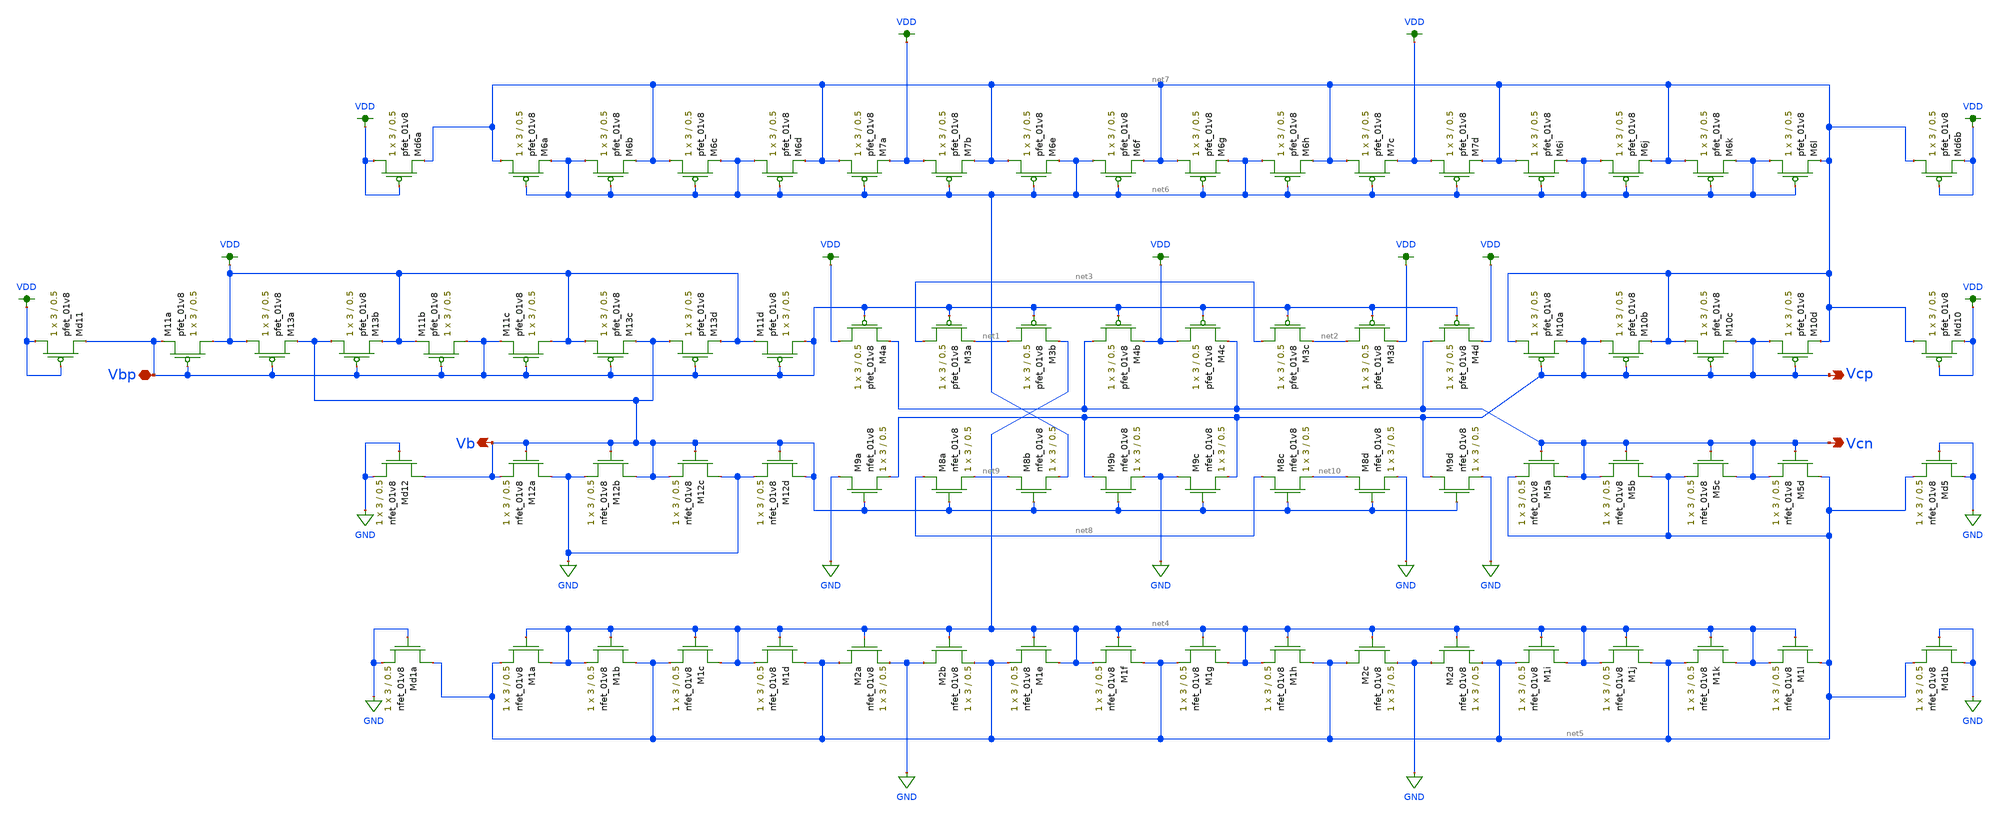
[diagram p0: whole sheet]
** sch_path: mp3/xschem/bias_layout.sch
**.subckt bias_layout Vcp Vbp Vcn Vb
*.opin Vcp
*.iopin Vbp
*.opin Vcn
*.opin Vb
XM1a net4 net4 net5 GND sky130_fd_pr__nfet_01v8 L=0.5 W=3 nf=1 ad='int((nf+1)/2) * W/nf * 0.29' as='int((nf+2)/2) * W/nf * 0.29'
+ pd='2*int((nf+1)/2) * (W/nf + 0.29)' ps='2*int((nf+2)/2) * (W/nf + 0.29)' nrd='0.29 / W' nrs='0.29 / W'
+ sa=0 sb=0 sd=0 mult=1 m=1
XM1b net5 net4 net4 GND sky130_fd_pr__nfet_01v8 L=0.5 W=3 nf=1 ad='int((nf+1)/2) * W/nf * 0.29' as='int((nf+2)/2) * W/nf * 0.29'
+ pd='2*int((nf+1)/2) * (W/nf + 0.29)' ps='2*int((nf+2)/2) * (W/nf + 0.29)' nrd='0.29 / W' nrs='0.29 / W'
+ sa=0 sb=0 sd=0 mult=1 m=1
XM1c net4 net4 net5 GND sky130_fd_pr__nfet_01v8 L=0.5 W=3 nf=1 ad='int((nf+1)/2) * W/nf * 0.29' as='int((nf+2)/2) * W/nf * 0.29'
+ pd='2*int((nf+1)/2) * (W/nf + 0.29)' ps='2*int((nf+2)/2) * (W/nf + 0.29)' nrd='0.29 / W' nrs='0.29 / W'
+ sa=0 sb=0 sd=0 mult=1 m=1
XM1d net5 net4 net4 GND sky130_fd_pr__nfet_01v8 L=0.5 W=3 nf=1 ad='int((nf+1)/2) * W/nf * 0.29' as='int((nf+2)/2) * W/nf * 0.29'
+ pd='2*int((nf+1)/2) * (W/nf + 0.29)' ps='2*int((nf+2)/2) * (W/nf + 0.29)' nrd='0.29 / W' nrs='0.29 / W'
+ sa=0 sb=0 sd=0 mult=1 m=1
XM2a net5 net4 GND GND sky130_fd_pr__nfet_01v8 L=0.5 W=3 nf=1 ad='int((nf+1)/2) * W/nf * 0.29' as='int((nf+2)/2) * W/nf * 0.29'
+ pd='2*int((nf+1)/2) * (W/nf + 0.29)' ps='2*int((nf+2)/2) * (W/nf + 0.29)' nrd='0.29 / W' nrs='0.29 / W'
+ sa=0 sb=0 sd=0 mult=1 m=1
XM2b GND net4 net5 GND sky130_fd_pr__nfet_01v8 L=0.5 W=3 nf=1 ad='int((nf+1)/2) * W/nf * 0.29' as='int((nf+2)/2) * W/nf * 0.29'
+ pd='2*int((nf+1)/2) * (W/nf + 0.29)' ps='2*int((nf+2)/2) * (W/nf + 0.29)' nrd='0.29 / W' nrs='0.29 / W'
+ sa=0 sb=0 sd=0 mult=1 m=1
XM2c net5 net4 GND GND sky130_fd_pr__nfet_01v8 L=0.5 W=3 nf=1 ad='int((nf+1)/2) * W/nf * 0.29' as='int((nf+2)/2) * W/nf * 0.29'
+ pd='2*int((nf+1)/2) * (W/nf + 0.29)' ps='2*int((nf+2)/2) * (W/nf + 0.29)' nrd='0.29 / W' nrs='0.29 / W'
+ sa=0 sb=0 sd=0 mult=1 m=1
XM2d GND net4 net5 GND sky130_fd_pr__nfet_01v8 L=0.5 W=3 nf=1 ad='int((nf+1)/2) * W/nf * 0.29' as='int((nf+2)/2) * W/nf * 0.29'
+ pd='2*int((nf+1)/2) * (W/nf + 0.29)' ps='2*int((nf+2)/2) * (W/nf + 0.29)' nrd='0.29 / W' nrs='0.29 / W'
+ sa=0 sb=0 sd=0 mult=1 m=1
XM3a net3 Vbp net1 VDD sky130_fd_pr__pfet_01v8 L=0.5 W=3 nf=1 ad='int((nf+1)/2) * W/nf * 0.29' as='int((nf+2)/2) * W/nf * 0.29'
+ pd='2*int((nf+1)/2) * (W/nf + 0.29)' ps='2*int((nf+2)/2) * (W/nf + 0.29)' nrd='0.29 / W' nrs='0.29 / W'
+ sa=0 sb=0 sd=0 mult=1 m=1
XM3b net1 Vbp net4 VDD sky130_fd_pr__pfet_01v8 L=0.5 W=3 nf=1 ad='int((nf+1)/2) * W/nf * 0.29' as='int((nf+2)/2) * W/nf * 0.29'
+ pd='2*int((nf+1)/2) * (W/nf + 0.29)' ps='2*int((nf+2)/2) * (W/nf + 0.29)' nrd='0.29 / W' nrs='0.29 / W'
+ sa=0 sb=0 sd=0 mult=1 m=1
XM3c net3 Vbp net2 VDD sky130_fd_pr__pfet_01v8 L=0.5 W=3 nf=1 ad='int((nf+1)/2) * W/nf * 0.29' as='int((nf+2)/2) * W/nf * 0.29'
+ pd='2*int((nf+1)/2) * (W/nf + 0.29)' ps='2*int((nf+2)/2) * (W/nf + 0.29)' nrd='0.29 / W' nrs='0.29 / W'
+ sa=0 sb=0 sd=0 mult=1 m=1
XM3d net2 Vbp VDD VDD sky130_fd_pr__pfet_01v8 L=0.5 W=3 nf=1 ad='int((nf+1)/2) * W/nf * 0.29' as='int((nf+2)/2) * W/nf * 0.29'
+ pd='2*int((nf+1)/2) * (W/nf + 0.29)' ps='2*int((nf+2)/2) * (W/nf + 0.29)' nrd='0.29 / W' nrs='0.29 / W'
+ sa=0 sb=0 sd=0 mult=1 m=1
XM4a VDD Vbp Vcn VDD sky130_fd_pr__pfet_01v8 L=0.5 W=3 nf=1 ad='int((nf+1)/2) * W/nf * 0.29' as='int((nf+2)/2) * W/nf * 0.29'
+ pd='2*int((nf+1)/2) * (W/nf + 0.29)' ps='2*int((nf+2)/2) * (W/nf + 0.29)' nrd='0.29 / W' nrs='0.29 / W'
+ sa=0 sb=0 sd=0 mult=1 m=1
XM4b Vcn Vbp VDD VDD sky130_fd_pr__pfet_01v8 L=0.5 W=3 nf=1 ad='int((nf+1)/2) * W/nf * 0.29' as='int((nf+2)/2) * W/nf * 0.29'
+ pd='2*int((nf+1)/2) * (W/nf + 0.29)' ps='2*int((nf+2)/2) * (W/nf + 0.29)' nrd='0.29 / W' nrs='0.29 / W'
+ sa=0 sb=0 sd=0 mult=1 m=1
XM4c VDD Vbp Vcn VDD sky130_fd_pr__pfet_01v8 L=0.5 W=3 nf=1 ad='int((nf+1)/2) * W/nf * 0.29' as='int((nf+2)/2) * W/nf * 0.29'
+ pd='2*int((nf+1)/2) * (W/nf + 0.29)' ps='2*int((nf+2)/2) * (W/nf + 0.29)' nrd='0.29 / W' nrs='0.29 / W'
+ sa=0 sb=0 sd=0 mult=1 m=1
XM4d Vcn Vbp VDD VDD sky130_fd_pr__pfet_01v8 L=0.5 W=3 nf=1 ad='int((nf+1)/2) * W/nf * 0.29' as='int((nf+2)/2) * W/nf * 0.29'
+ pd='2*int((nf+1)/2) * (W/nf + 0.29)' ps='2*int((nf+2)/2) * (W/nf + 0.29)' nrd='0.29 / W' nrs='0.29 / W'
+ sa=0 sb=0 sd=0 mult=1 m=1
XM11a VDD Vbp Vbp VDD sky130_fd_pr__pfet_01v8 L=0.5 W=3 nf=1 ad='int((nf+1)/2) * W/nf * 0.29' as='int((nf+2)/2) * W/nf * 0.29'
+ pd='2*int((nf+1)/2) * (W/nf + 0.29)' ps='2*int((nf+2)/2) * (W/nf + 0.29)' nrd='0.29 / W' nrs='0.29 / W'
+ sa=0 sb=0 sd=0 mult=1 m=1
XM11b Vbp Vbp VDD VDD sky130_fd_pr__pfet_01v8 L=0.5 W=3 nf=1 ad='int((nf+1)/2) * W/nf * 0.29' as='int((nf+2)/2) * W/nf * 0.29'
+ pd='2*int((nf+1)/2) * (W/nf + 0.29)' ps='2*int((nf+2)/2) * (W/nf + 0.29)' nrd='0.29 / W' nrs='0.29 / W'
+ sa=0 sb=0 sd=0 mult=1 m=1
XM11c VDD Vbp Vbp VDD sky130_fd_pr__pfet_01v8 L=0.5 W=3 nf=1 ad='int((nf+1)/2) * W/nf * 0.29' as='int((nf+2)/2) * W/nf * 0.29'
+ pd='2*int((nf+1)/2) * (W/nf + 0.29)' ps='2*int((nf+2)/2) * (W/nf + 0.29)' nrd='0.29 / W' nrs='0.29 / W'
+ sa=0 sb=0 sd=0 mult=1 m=1
XM11d Vbp Vbp VDD VDD sky130_fd_pr__pfet_01v8 L=0.5 W=3 nf=1 ad='int((nf+1)/2) * W/nf * 0.29' as='int((nf+2)/2) * W/nf * 0.29'
+ pd='2*int((nf+1)/2) * (W/nf + 0.29)' ps='2*int((nf+2)/2) * (W/nf + 0.29)' nrd='0.29 / W' nrs='0.29 / W'
+ sa=0 sb=0 sd=0 mult=1 m=1
XM5a Vcn Vcn net5 GND sky130_fd_pr__nfet_01v8 L=0.5 W=3 nf=1 ad='int((nf+1)/2) * W/nf * 0.29' as='int((nf+2)/2) * W/nf * 0.29'
+ pd='2*int((nf+1)/2) * (W/nf + 0.29)' ps='2*int((nf+2)/2) * (W/nf + 0.29)' nrd='0.29 / W' nrs='0.29 / W'
+ sa=0 sb=0 sd=0 mult=1 m=1
XM5b net5 Vcn Vcn GND sky130_fd_pr__nfet_01v8 L=0.5 W=3 nf=1 ad='int((nf+1)/2) * W/nf * 0.29' as='int((nf+2)/2) * W/nf * 0.29'
+ pd='2*int((nf+1)/2) * (W/nf + 0.29)' ps='2*int((nf+2)/2) * (W/nf + 0.29)' nrd='0.29 / W' nrs='0.29 / W'
+ sa=0 sb=0 sd=0 mult=1 m=1
XM5c Vcn Vcn net5 GND sky130_fd_pr__nfet_01v8 L=0.5 W=3 nf=1 ad='int((nf+1)/2) * W/nf * 0.29' as='int((nf+2)/2) * W/nf * 0.29'
+ pd='2*int((nf+1)/2) * (W/nf + 0.29)' ps='2*int((nf+2)/2) * (W/nf + 0.29)' nrd='0.29 / W' nrs='0.29 / W'
+ sa=0 sb=0 sd=0 mult=1 m=1
XM5d net5 Vcn Vcn GND sky130_fd_pr__nfet_01v8 L=0.5 W=3 nf=1 ad='int((nf+1)/2) * W/nf * 0.29' as='int((nf+2)/2) * W/nf * 0.29'
+ pd='2*int((nf+1)/2) * (W/nf + 0.29)' ps='2*int((nf+2)/2) * (W/nf + 0.29)' nrd='0.29 / W' nrs='0.29 / W'
+ sa=0 sb=0 sd=0 mult=1 m=1
XM8a net8 Vb net9 GND sky130_fd_pr__nfet_01v8 L=0.5 W=3 nf=1 ad='int((nf+1)/2) * W/nf * 0.29' as='int((nf+2)/2) * W/nf * 0.29'
+ pd='2*int((nf+1)/2) * (W/nf + 0.29)' ps='2*int((nf+2)/2) * (W/nf + 0.29)' nrd='0.29 / W' nrs='0.29 / W'
+ sa=0 sb=0 sd=0 mult=1 m=1
XM8b net9 Vb net6 GND sky130_fd_pr__nfet_01v8 L=0.5 W=3 nf=1 ad='int((nf+1)/2) * W/nf * 0.29' as='int((nf+2)/2) * W/nf * 0.29'
+ pd='2*int((nf+1)/2) * (W/nf + 0.29)' ps='2*int((nf+2)/2) * (W/nf + 0.29)' nrd='0.29 / W' nrs='0.29 / W'
+ sa=0 sb=0 sd=0 mult=1 m=1
XM8c net8 Vb net10 GND sky130_fd_pr__nfet_01v8 L=0.5 W=3 nf=1 ad='int((nf+1)/2) * W/nf * 0.29' as='int((nf+2)/2) * W/nf * 0.29'
+ pd='2*int((nf+1)/2) * (W/nf + 0.29)' ps='2*int((nf+2)/2) * (W/nf + 0.29)' nrd='0.29 / W' nrs='0.29 / W'
+ sa=0 sb=0 sd=0 mult=1 m=1
XM8d net10 Vb GND GND sky130_fd_pr__nfet_01v8 L=0.5 W=3 nf=1 ad='int((nf+1)/2) * W/nf * 0.29' as='int((nf+2)/2) * W/nf * 0.29'
+ pd='2*int((nf+1)/2) * (W/nf + 0.29)' ps='2*int((nf+2)/2) * (W/nf + 0.29)' nrd='0.29 / W' nrs='0.29 / W'
+ sa=0 sb=0 sd=0 mult=1 m=1
XM6a net7 net6 net6 VDD sky130_fd_pr__pfet_01v8 L=0.5 W=3 nf=1 ad='int((nf+1)/2) * W/nf * 0.29' as='int((nf+2)/2) * W/nf * 0.29'
+ pd='2*int((nf+1)/2) * (W/nf + 0.29)' ps='2*int((nf+2)/2) * (W/nf + 0.29)' nrd='0.29 / W' nrs='0.29 / W'
+ sa=0 sb=0 sd=0 mult=1 m=1
XM6b net6 net6 net7 VDD sky130_fd_pr__pfet_01v8 L=0.5 W=3 nf=1 ad='int((nf+1)/2) * W/nf * 0.29' as='int((nf+2)/2) * W/nf * 0.29'
+ pd='2*int((nf+1)/2) * (W/nf + 0.29)' ps='2*int((nf+2)/2) * (W/nf + 0.29)' nrd='0.29 / W' nrs='0.29 / W'
+ sa=0 sb=0 sd=0 mult=1 m=1
XM6c net7 net6 net6 VDD sky130_fd_pr__pfet_01v8 L=0.5 W=3 nf=1 ad='int((nf+1)/2) * W/nf * 0.29' as='int((nf+2)/2) * W/nf * 0.29'
+ pd='2*int((nf+1)/2) * (W/nf + 0.29)' ps='2*int((nf+2)/2) * (W/nf + 0.29)' nrd='0.29 / W' nrs='0.29 / W'
+ sa=0 sb=0 sd=0 mult=1 m=1
XM6d net6 net6 net7 VDD sky130_fd_pr__pfet_01v8 L=0.5 W=3 nf=1 ad='int((nf+1)/2) * W/nf * 0.29' as='int((nf+2)/2) * W/nf * 0.29'
+ pd='2*int((nf+1)/2) * (W/nf + 0.29)' ps='2*int((nf+2)/2) * (W/nf + 0.29)' nrd='0.29 / W' nrs='0.29 / W'
+ sa=0 sb=0 sd=0 mult=1 m=1
XM7a net7 net6 VDD VDD sky130_fd_pr__pfet_01v8 L=0.5 W=3 nf=1 ad='int((nf+1)/2) * W/nf * 0.29' as='int((nf+2)/2) * W/nf * 0.29'
+ pd='2*int((nf+1)/2) * (W/nf + 0.29)' ps='2*int((nf+2)/2) * (W/nf + 0.29)' nrd='0.29 / W' nrs='0.29 / W'
+ sa=0 sb=0 sd=0 mult=1 m=1
XM7b VDD net6 net7 VDD sky130_fd_pr__pfet_01v8 L=0.5 W=3 nf=1 ad='int((nf+1)/2) * W/nf * 0.29' as='int((nf+2)/2) * W/nf * 0.29'
+ pd='2*int((nf+1)/2) * (W/nf + 0.29)' ps='2*int((nf+2)/2) * (W/nf + 0.29)' nrd='0.29 / W' nrs='0.29 / W'
+ sa=0 sb=0 sd=0 mult=1 m=1
XM7c net7 net6 VDD VDD sky130_fd_pr__pfet_01v8 L=0.5 W=3 nf=1 ad='int((nf+1)/2) * W/nf * 0.29' as='int((nf+2)/2) * W/nf * 0.29'
+ pd='2*int((nf+1)/2) * (W/nf + 0.29)' ps='2*int((nf+2)/2) * (W/nf + 0.29)' nrd='0.29 / W' nrs='0.29 / W'
+ sa=0 sb=0 sd=0 mult=1 m=1
XM7d VDD net6 net7 VDD sky130_fd_pr__pfet_01v8 L=0.5 W=3 nf=1 ad='int((nf+1)/2) * W/nf * 0.29' as='int((nf+2)/2) * W/nf * 0.29'
+ pd='2*int((nf+1)/2) * (W/nf + 0.29)' ps='2*int((nf+2)/2) * (W/nf + 0.29)' nrd='0.29 / W' nrs='0.29 / W'
+ sa=0 sb=0 sd=0 mult=1 m=1
XM10d Vcp Vcp net7 VDD sky130_fd_pr__pfet_01v8 L=0.5 W=3 nf=1 ad='int((nf+1)/2) * W/nf * 0.29' as='int((nf+2)/2) * W/nf * 0.29'
+ pd='2*int((nf+1)/2) * (W/nf + 0.29)' ps='2*int((nf+2)/2) * (W/nf + 0.29)' nrd='0.29 / W' nrs='0.29 / W'
+ sa=0 sb=0 sd=0 mult=1 m=1
XM10c net7 Vcp Vcp VDD sky130_fd_pr__pfet_01v8 L=0.5 W=3 nf=1 ad='int((nf+1)/2) * W/nf * 0.29' as='int((nf+2)/2) * W/nf * 0.29'
+ pd='2*int((nf+1)/2) * (W/nf + 0.29)' ps='2*int((nf+2)/2) * (W/nf + 0.29)' nrd='0.29 / W' nrs='0.29 / W'
+ sa=0 sb=0 sd=0 mult=1 m=1
XM10b Vcp Vcp net7 VDD sky130_fd_pr__pfet_01v8 L=0.5 W=3 nf=1 ad='int((nf+1)/2) * W/nf * 0.29' as='int((nf+2)/2) * W/nf * 0.29'
+ pd='2*int((nf+1)/2) * (W/nf + 0.29)' ps='2*int((nf+2)/2) * (W/nf + 0.29)' nrd='0.29 / W' nrs='0.29 / W'
+ sa=0 sb=0 sd=0 mult=1 m=1
XM10a net7 Vcp Vcp VDD sky130_fd_pr__pfet_01v8 L=0.5 W=3 nf=1 ad='int((nf+1)/2) * W/nf * 0.29' as='int((nf+2)/2) * W/nf * 0.29'
+ pd='2*int((nf+1)/2) * (W/nf + 0.29)' ps='2*int((nf+2)/2) * (W/nf + 0.29)' nrd='0.29 / W' nrs='0.29 / W'
+ sa=0 sb=0 sd=0 mult=1 m=1
XM9a GND Vb Vcp GND sky130_fd_pr__nfet_01v8 L=0.5 W=3 nf=1 ad='int((nf+1)/2) * W/nf * 0.29' as='int((nf+2)/2) * W/nf * 0.29'
+ pd='2*int((nf+1)/2) * (W/nf + 0.29)' ps='2*int((nf+2)/2) * (W/nf + 0.29)' nrd='0.29 / W' nrs='0.29 / W'
+ sa=0 sb=0 sd=0 mult=1 m=1
XM9b Vcp Vb GND GND sky130_fd_pr__nfet_01v8 L=0.5 W=3 nf=1 ad='int((nf+1)/2) * W/nf * 0.29' as='int((nf+2)/2) * W/nf * 0.29'
+ pd='2*int((nf+1)/2) * (W/nf + 0.29)' ps='2*int((nf+2)/2) * (W/nf + 0.29)' nrd='0.29 / W' nrs='0.29 / W'
+ sa=0 sb=0 sd=0 mult=1 m=1
XM9c GND Vb Vcp GND sky130_fd_pr__nfet_01v8 L=0.5 W=3 nf=1 ad='int((nf+1)/2) * W/nf * 0.29' as='int((nf+2)/2) * W/nf * 0.29'
+ pd='2*int((nf+1)/2) * (W/nf + 0.29)' ps='2*int((nf+2)/2) * (W/nf + 0.29)' nrd='0.29 / W' nrs='0.29 / W'
+ sa=0 sb=0 sd=0 mult=1 m=1
XM9d Vcp Vb GND GND sky130_fd_pr__nfet_01v8 L=0.5 W=3 nf=1 ad='int((nf+1)/2) * W/nf * 0.29' as='int((nf+2)/2) * W/nf * 0.29'
+ pd='2*int((nf+1)/2) * (W/nf + 0.29)' ps='2*int((nf+2)/2) * (W/nf + 0.29)' nrd='0.29 / W' nrs='0.29 / W'
+ sa=0 sb=0 sd=0 mult=1 m=1
XM12a GND Vb Vb GND sky130_fd_pr__nfet_01v8 L=0.5 W=3 nf=1 ad='int((nf+1)/2) * W/nf * 0.29' as='int((nf+2)/2) * W/nf * 0.29'
+ pd='2*int((nf+1)/2) * (W/nf + 0.29)' ps='2*int((nf+2)/2) * (W/nf + 0.29)' nrd='0.29 / W' nrs='0.29 / W'
+ sa=0 sb=0 sd=0 mult=1 m=1
XM12b Vb Vb GND GND sky130_fd_pr__nfet_01v8 L=0.5 W=3 nf=1 ad='int((nf+1)/2) * W/nf * 0.29' as='int((nf+2)/2) * W/nf * 0.29'
+ pd='2*int((nf+1)/2) * (W/nf + 0.29)' ps='2*int((nf+2)/2) * (W/nf + 0.29)' nrd='0.29 / W' nrs='0.29 / W'
+ sa=0 sb=0 sd=0 mult=1 m=1
XM12c GND Vb Vb GND sky130_fd_pr__nfet_01v8 L=0.5 W=3 nf=1 ad='int((nf+1)/2) * W/nf * 0.29' as='int((nf+2)/2) * W/nf * 0.29'
+ pd='2*int((nf+1)/2) * (W/nf + 0.29)' ps='2*int((nf+2)/2) * (W/nf + 0.29)' nrd='0.29 / W' nrs='0.29 / W'
+ sa=0 sb=0 sd=0 mult=1 m=1
XM12d Vb Vb GND GND sky130_fd_pr__nfet_01v8 L=0.5 W=3 nf=1 ad='int((nf+1)/2) * W/nf * 0.29' as='int((nf+2)/2) * W/nf * 0.29'
+ pd='2*int((nf+1)/2) * (W/nf + 0.29)' ps='2*int((nf+2)/2) * (W/nf + 0.29)' nrd='0.29 / W' nrs='0.29 / W'
+ sa=0 sb=0 sd=0 mult=1 m=1
XM13d Vb Vbp VDD VDD sky130_fd_pr__pfet_01v8 L=0.5 W=3 nf=1 ad='int((nf+1)/2) * W/nf * 0.29' as='int((nf+2)/2) * W/nf * 0.29'
+ pd='2*int((nf+1)/2) * (W/nf + 0.29)' ps='2*int((nf+2)/2) * (W/nf + 0.29)' nrd='0.29 / W' nrs='0.29 / W'
+ sa=0 sb=0 sd=0 mult=1 m=1
XM13c VDD Vbp Vb VDD sky130_fd_pr__pfet_01v8 L=0.5 W=3 nf=1 ad='int((nf+1)/2) * W/nf * 0.29' as='int((nf+2)/2) * W/nf * 0.29'
+ pd='2*int((nf+1)/2) * (W/nf + 0.29)' ps='2*int((nf+2)/2) * (W/nf + 0.29)' nrd='0.29 / W' nrs='0.29 / W'
+ sa=0 sb=0 sd=0 mult=1 m=1
XM13b Vb Vbp VDD VDD sky130_fd_pr__pfet_01v8 L=0.5 W=3 nf=1 ad='int((nf+1)/2) * W/nf * 0.29' as='int((nf+2)/2) * W/nf * 0.29'
+ pd='2*int((nf+1)/2) * (W/nf + 0.29)' ps='2*int((nf+2)/2) * (W/nf + 0.29)' nrd='0.29 / W' nrs='0.29 / W'
+ sa=0 sb=0 sd=0 mult=1 m=1
XM13a VDD Vbp Vb VDD sky130_fd_pr__pfet_01v8 L=0.5 W=3 nf=1 ad='int((nf+1)/2) * W/nf * 0.29' as='int((nf+2)/2) * W/nf * 0.29'
+ pd='2*int((nf+1)/2) * (W/nf + 0.29)' ps='2*int((nf+2)/2) * (W/nf + 0.29)' nrd='0.29 / W' nrs='0.29 / W'
+ sa=0 sb=0 sd=0 mult=1 m=1
XM1e net4 net4 net5 GND sky130_fd_pr__nfet_01v8 L=0.5 W=3 nf=1 ad='int((nf+1)/2) * W/nf * 0.29' as='int((nf+2)/2) * W/nf * 0.29'
+ pd='2*int((nf+1)/2) * (W/nf + 0.29)' ps='2*int((nf+2)/2) * (W/nf + 0.29)' nrd='0.29 / W' nrs='0.29 / W'
+ sa=0 sb=0 sd=0 mult=1 m=1
XM1f net5 net4 net4 GND sky130_fd_pr__nfet_01v8 L=0.5 W=3 nf=1 ad='int((nf+1)/2) * W/nf * 0.29' as='int((nf+2)/2) * W/nf * 0.29'
+ pd='2*int((nf+1)/2) * (W/nf + 0.29)' ps='2*int((nf+2)/2) * (W/nf + 0.29)' nrd='0.29 / W' nrs='0.29 / W'
+ sa=0 sb=0 sd=0 mult=1 m=1
XM1g net4 net4 net5 GND sky130_fd_pr__nfet_01v8 L=0.5 W=3 nf=1 ad='int((nf+1)/2) * W/nf * 0.29' as='int((nf+2)/2) * W/nf * 0.29'
+ pd='2*int((nf+1)/2) * (W/nf + 0.29)' ps='2*int((nf+2)/2) * (W/nf + 0.29)' nrd='0.29 / W' nrs='0.29 / W'
+ sa=0 sb=0 sd=0 mult=1 m=1
XM1h net5 net4 net4 GND sky130_fd_pr__nfet_01v8 L=0.5 W=3 nf=1 ad='int((nf+1)/2) * W/nf * 0.29' as='int((nf+2)/2) * W/nf * 0.29'
+ pd='2*int((nf+1)/2) * (W/nf + 0.29)' ps='2*int((nf+2)/2) * (W/nf + 0.29)' nrd='0.29 / W' nrs='0.29 / W'
+ sa=0 sb=0 sd=0 mult=1 m=1
XM6e net7 net6 net6 VDD sky130_fd_pr__pfet_01v8 L=0.5 W=3 nf=1 ad='int((nf+1)/2) * W/nf * 0.29' as='int((nf+2)/2) * W/nf * 0.29'
+ pd='2*int((nf+1)/2) * (W/nf + 0.29)' ps='2*int((nf+2)/2) * (W/nf + 0.29)' nrd='0.29 / W' nrs='0.29 / W'
+ sa=0 sb=0 sd=0 mult=1 m=1
XM6f net6 net6 net7 VDD sky130_fd_pr__pfet_01v8 L=0.5 W=3 nf=1 ad='int((nf+1)/2) * W/nf * 0.29' as='int((nf+2)/2) * W/nf * 0.29'
+ pd='2*int((nf+1)/2) * (W/nf + 0.29)' ps='2*int((nf+2)/2) * (W/nf + 0.29)' nrd='0.29 / W' nrs='0.29 / W'
+ sa=0 sb=0 sd=0 mult=1 m=1
XM6g net7 net6 net6 VDD sky130_fd_pr__pfet_01v8 L=0.5 W=3 nf=1 ad='int((nf+1)/2) * W/nf * 0.29' as='int((nf+2)/2) * W/nf * 0.29'
+ pd='2*int((nf+1)/2) * (W/nf + 0.29)' ps='2*int((nf+2)/2) * (W/nf + 0.29)' nrd='0.29 / W' nrs='0.29 / W'
+ sa=0 sb=0 sd=0 mult=1 m=1
XM6h net6 net6 net7 VDD sky130_fd_pr__pfet_01v8 L=0.5 W=3 nf=1 ad='int((nf+1)/2) * W/nf * 0.29' as='int((nf+2)/2) * W/nf * 0.29'
+ pd='2*int((nf+1)/2) * (W/nf + 0.29)' ps='2*int((nf+2)/2) * (W/nf + 0.29)' nrd='0.29 / W' nrs='0.29 / W'
+ sa=0 sb=0 sd=0 mult=1 m=1
XM1i net4 net4 net5 GND sky130_fd_pr__nfet_01v8 L=0.5 W=3 nf=1 ad='int((nf+1)/2) * W/nf * 0.29' as='int((nf+2)/2) * W/nf * 0.29'
+ pd='2*int((nf+1)/2) * (W/nf + 0.29)' ps='2*int((nf+2)/2) * (W/nf + 0.29)' nrd='0.29 / W' nrs='0.29 / W'
+ sa=0 sb=0 sd=0 mult=1 m=1
XM1j net5 net4 net4 GND sky130_fd_pr__nfet_01v8 L=0.5 W=3 nf=1 ad='int((nf+1)/2) * W/nf * 0.29' as='int((nf+2)/2) * W/nf * 0.29'
+ pd='2*int((nf+1)/2) * (W/nf + 0.29)' ps='2*int((nf+2)/2) * (W/nf + 0.29)' nrd='0.29 / W' nrs='0.29 / W'
+ sa=0 sb=0 sd=0 mult=1 m=1
XM1k net4 net4 net5 GND sky130_fd_pr__nfet_01v8 L=0.5 W=3 nf=1 ad='int((nf+1)/2) * W/nf * 0.29' as='int((nf+2)/2) * W/nf * 0.29'
+ pd='2*int((nf+1)/2) * (W/nf + 0.29)' ps='2*int((nf+2)/2) * (W/nf + 0.29)' nrd='0.29 / W' nrs='0.29 / W'
+ sa=0 sb=0 sd=0 mult=1 m=1
XM1l net5 net4 net4 GND sky130_fd_pr__nfet_01v8 L=0.5 W=3 nf=1 ad='int((nf+1)/2) * W/nf * 0.29' as='int((nf+2)/2) * W/nf * 0.29'
+ pd='2*int((nf+1)/2) * (W/nf + 0.29)' ps='2*int((nf+2)/2) * (W/nf + 0.29)' nrd='0.29 / W' nrs='0.29 / W'
+ sa=0 sb=0 sd=0 mult=1 m=1
XM6i net7 net6 net6 VDD sky130_fd_pr__pfet_01v8 L=0.5 W=3 nf=1 ad='int((nf+1)/2) * W/nf * 0.29' as='int((nf+2)/2) * W/nf * 0.29'
+ pd='2*int((nf+1)/2) * (W/nf + 0.29)' ps='2*int((nf+2)/2) * (W/nf + 0.29)' nrd='0.29 / W' nrs='0.29 / W'
+ sa=0 sb=0 sd=0 mult=1 m=1
XM6j net6 net6 net7 VDD sky130_fd_pr__pfet_01v8 L=0.5 W=3 nf=1 ad='int((nf+1)/2) * W/nf * 0.29' as='int((nf+2)/2) * W/nf * 0.29'
+ pd='2*int((nf+1)/2) * (W/nf + 0.29)' ps='2*int((nf+2)/2) * (W/nf + 0.29)' nrd='0.29 / W' nrs='0.29 / W'
+ sa=0 sb=0 sd=0 mult=1 m=1
XM6k net7 net6 net6 VDD sky130_fd_pr__pfet_01v8 L=0.5 W=3 nf=1 ad='int((nf+1)/2) * W/nf * 0.29' as='int((nf+2)/2) * W/nf * 0.29'
+ pd='2*int((nf+1)/2) * (W/nf + 0.29)' ps='2*int((nf+2)/2) * (W/nf + 0.29)' nrd='0.29 / W' nrs='0.29 / W'
+ sa=0 sb=0 sd=0 mult=1 m=1
XM6l net6 net6 net7 VDD sky130_fd_pr__pfet_01v8 L=0.5 W=3 nf=1 ad='int((nf+1)/2) * W/nf * 0.29' as='int((nf+2)/2) * W/nf * 0.29'
+ pd='2*int((nf+1)/2) * (W/nf + 0.29)' ps='2*int((nf+2)/2) * (W/nf + 0.29)' nrd='0.29 / W' nrs='0.29 / W'
+ sa=0 sb=0 sd=0 mult=1 m=1
XMd6b net7 VDD VDD VDD sky130_fd_pr__pfet_01v8 L=0.5 W=3 nf=1 ad='int((nf+1)/2) * W/nf * 0.29' as='int((nf+2)/2) * W/nf * 0.29'
+ pd='2*int((nf+1)/2) * (W/nf + 0.29)' ps='2*int((nf+2)/2) * (W/nf + 0.29)' nrd='0.29 / W' nrs='0.29 / W'
+ sa=0 sb=0 sd=0 mult=1 m=1
XMd10 net7 VDD VDD VDD sky130_fd_pr__pfet_01v8 L=0.5 W=3 nf=1 ad='int((nf+1)/2) * W/nf * 0.29' as='int((nf+2)/2) * W/nf * 0.29'
+ pd='2*int((nf+1)/2) * (W/nf + 0.29)' ps='2*int((nf+2)/2) * (W/nf + 0.29)' nrd='0.29 / W' nrs='0.29 / W'
+ sa=0 sb=0 sd=0 mult=1 m=1
XMd5 GND GND net5 GND sky130_fd_pr__nfet_01v8 L=0.5 W=3 nf=1 ad='int((nf+1)/2) * W/nf * 0.29' as='int((nf+2)/2) * W/nf * 0.29'
+ pd='2*int((nf+1)/2) * (W/nf + 0.29)' ps='2*int((nf+2)/2) * (W/nf + 0.29)' nrd='0.29 / W' nrs='0.29 / W'
+ sa=0 sb=0 sd=0 mult=1 m=1
XMd1b GND GND net5 GND sky130_fd_pr__nfet_01v8 L=0.5 W=3 nf=1 ad='int((nf+1)/2) * W/nf * 0.29' as='int((nf+2)/2) * W/nf * 0.29'
+ pd='2*int((nf+1)/2) * (W/nf + 0.29)' ps='2*int((nf+2)/2) * (W/nf + 0.29)' nrd='0.29 / W' nrs='0.29 / W'
+ sa=0 sb=0 sd=0 mult=1 m=1
XMd6a VDD VDD net7 VDD sky130_fd_pr__pfet_01v8 L=0.5 W=3 nf=1 ad='int((nf+1)/2) * W/nf * 0.29' as='int((nf+2)/2) * W/nf * 0.29'
+ pd='2*int((nf+1)/2) * (W/nf + 0.29)' ps='2*int((nf+2)/2) * (W/nf + 0.29)' nrd='0.29 / W' nrs='0.29 / W'
+ sa=0 sb=0 sd=0 mult=1 m=1
XMd11 VDD VDD Vbp VDD sky130_fd_pr__pfet_01v8 L=0.5 W=3 nf=1 ad='int((nf+1)/2) * W/nf * 0.29' as='int((nf+2)/2) * W/nf * 0.29'
+ pd='2*int((nf+1)/2) * (W/nf + 0.29)' ps='2*int((nf+2)/2) * (W/nf + 0.29)' nrd='0.29 / W' nrs='0.29 / W'
+ sa=0 sb=0 sd=0 mult=1 m=1
XMd1a net5 GND GND GND sky130_fd_pr__nfet_01v8 L=0.5 W=3 nf=1 ad='int((nf+1)/2) * W/nf * 0.29' as='int((nf+2)/2) * W/nf * 0.29'
+ pd='2*int((nf+1)/2) * (W/nf + 0.29)' ps='2*int((nf+2)/2) * (W/nf + 0.29)' nrd='0.29 / W' nrs='0.29 / W'
+ sa=0 sb=0 sd=0 mult=1 m=1
XMd12 Vb GND GND GND sky130_fd_pr__nfet_01v8 L=0.5 W=3 nf=1 ad='int((nf+1)/2) * W/nf * 0.29' as='int((nf+2)/2) * W/nf * 0.29'
+ pd='2*int((nf+1)/2) * (W/nf + 0.29)' ps='2*int((nf+2)/2) * (W/nf + 0.29)' nrd='0.29 / W' nrs='0.29 / W'
+ sa=0 sb=0 sd=0 mult=1 m=1
**.ends
.GLOBAL VDD
.GLOBAL GND
.end
